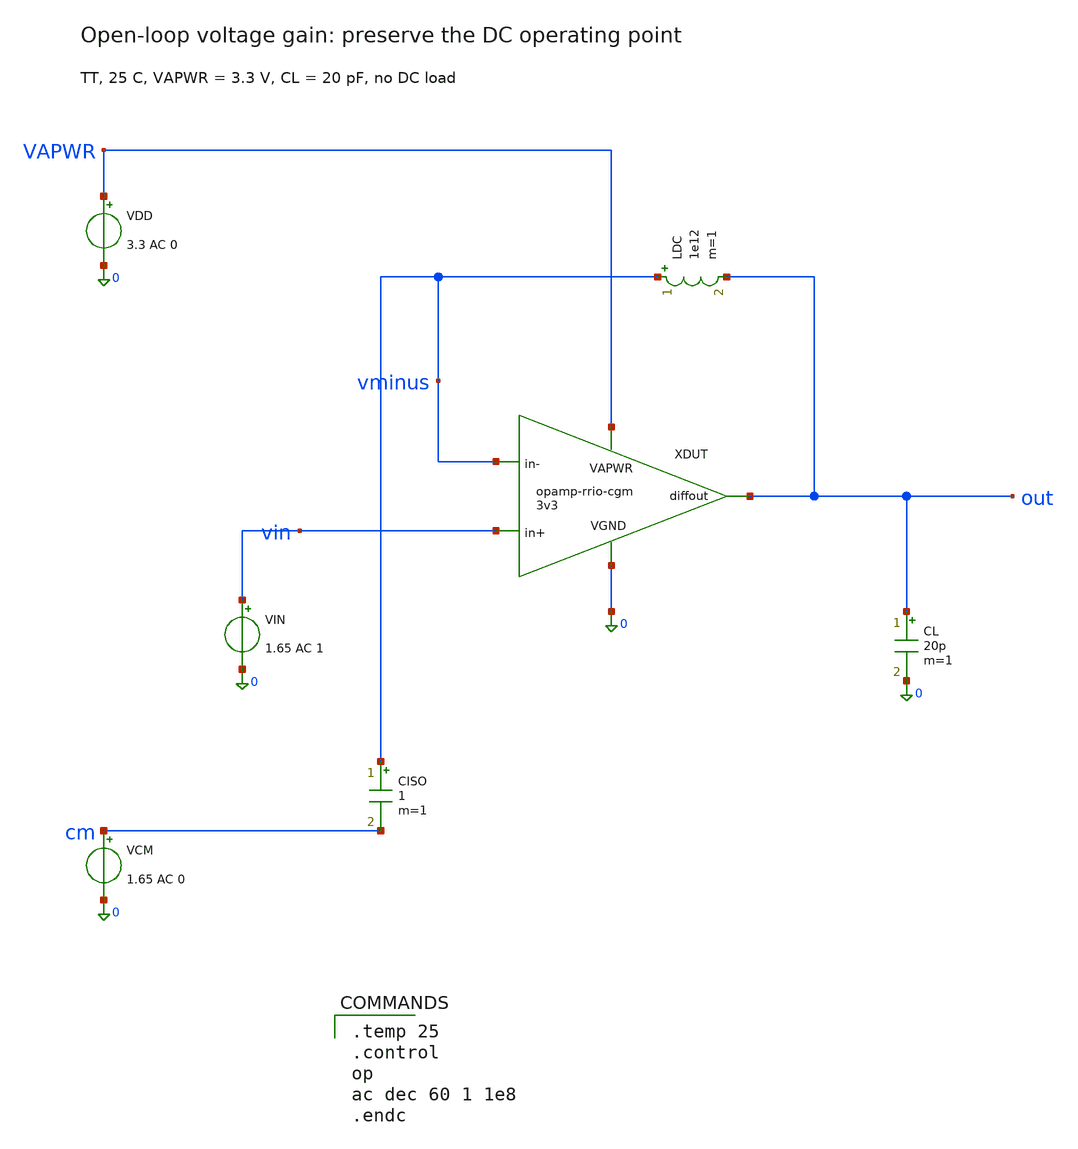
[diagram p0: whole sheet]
** sch_path: docs/simulation/xschem/bench-open.sch
**.subckt bench-open
XDUT VAPWR out vin vminus 0 opamp-rrio-cgm-3v3
VDD VAPWR 0 3.3 AC 0
VIN vin 0 1.65 AC 1
CL out 0 20p m=1
LDC vminus out 1e12 m=1
CISO vminus cm 1 m=1
VCM cm 0 1.65 AC 0
**** begin user architecture code
 .lib $::SKYWATER_MODELS/sky130.lib.spice tt

.temp 25
.control
op
ac dec 60 1 1e8
.endc

**** end user architecture code
**.ends
.end
